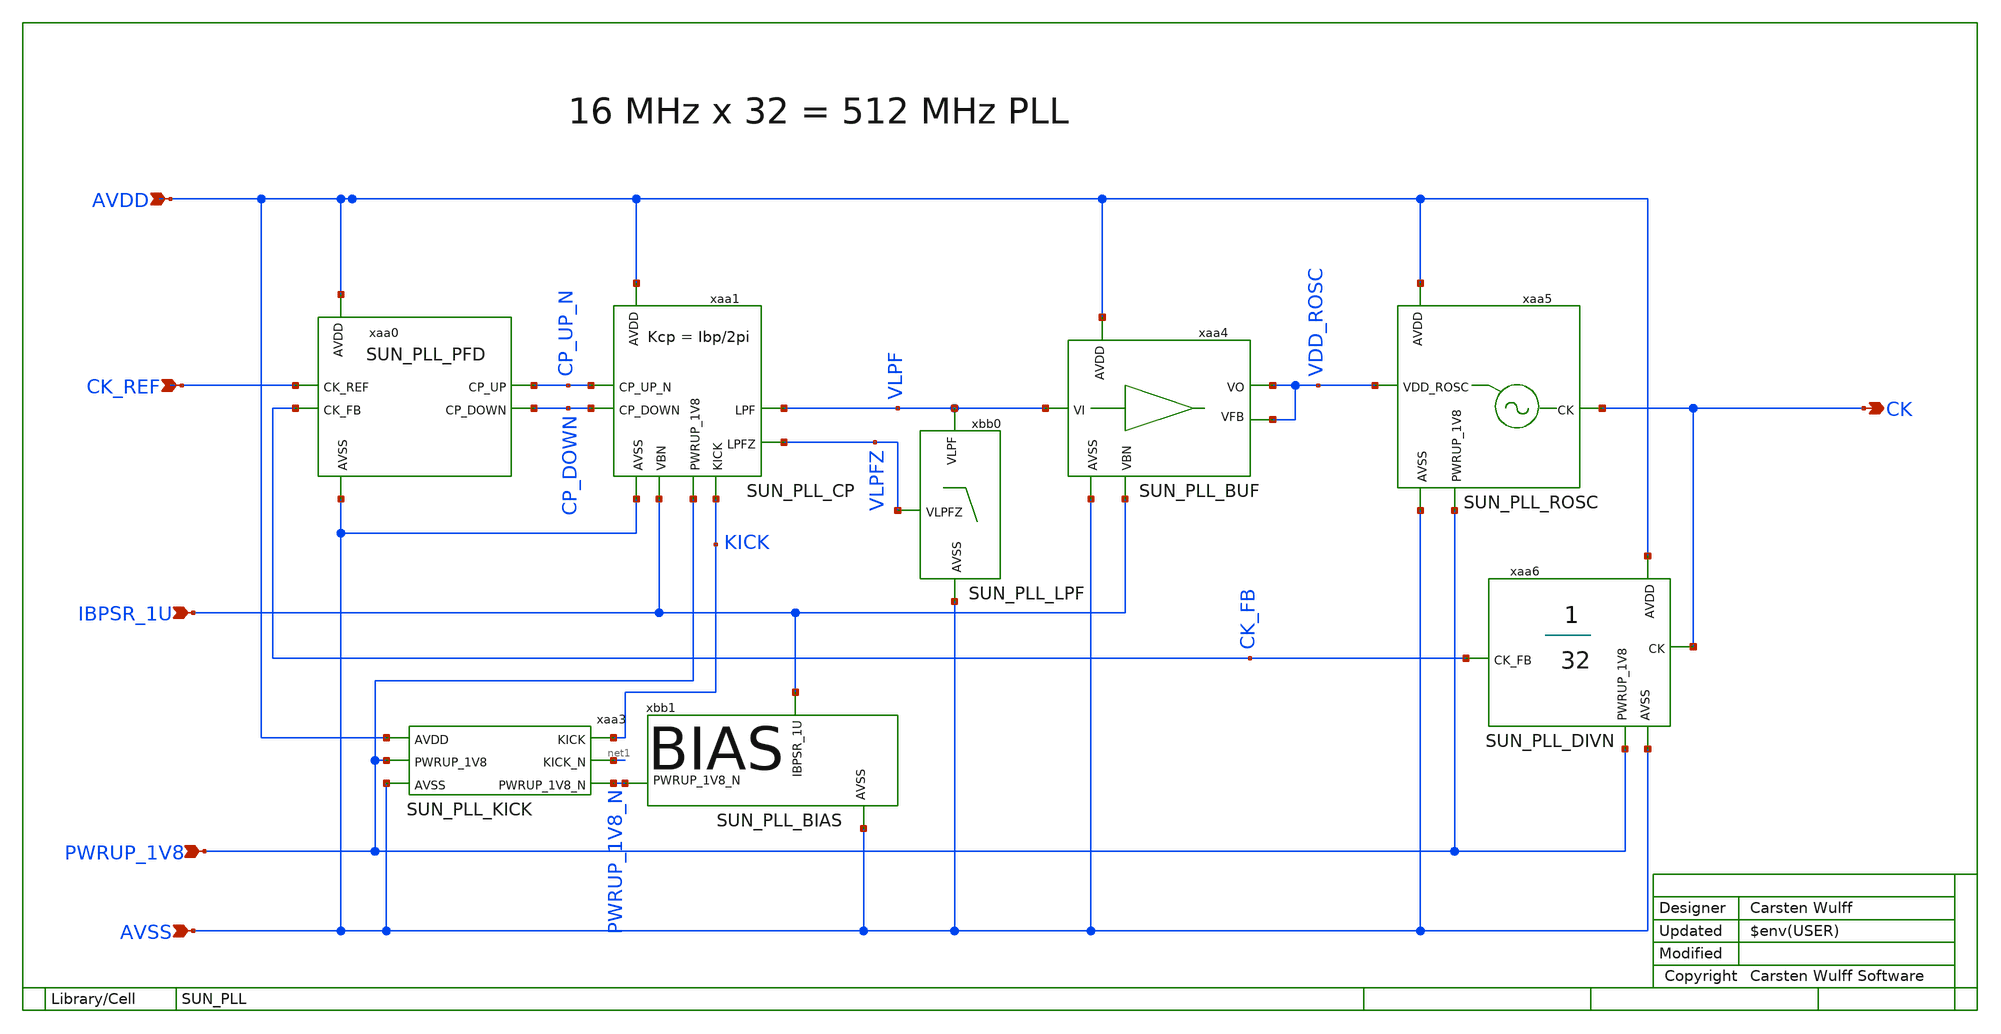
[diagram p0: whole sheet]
** sch_path: ip/sun_pll_sky130nm/design/SUN_PLL_SKY130NM/SUN_PLL.sch
**.subckt SUN_PLL AVDD AVSS PWRUP_1V8 CK_REF CK IBPSR_1U
*.ipin AVDD
*.ipin AVSS
*.ipin PWRUP_1V8
*.ipin CK_REF
*.opin CK
*.ipin IBPSR_1U
xaa5 AVDD CK VDD_ROSC PWRUP_1V8 AVSS SUN_PLL_ROSC xoffset=5 yoffset=0 angle=0
xaa6 AVDD CK_FB CK PWRUP_1V8 AVSS SUN_PLL_DIVN xoffset=-310 yoffset=0 angle=0
xbb1 IBPSR_1U PWRUP_1V8_N AVSS SUN_PLL_BIAS xoffset=5 yoffset=0 angle=0
xaa4 AVDD VDD_ROSC VLPF VDD_ROSC IBPSR_1U AVSS SUN_PLL_BUF xoffset=0 yoffset=0 angle=0
xbb0 VLPFZ AVSS VLPF SUN_PLL_LPF xoffset=0 yoffset=5 angle=0
xaa1 AVDD CP_UP_N VLPF CP_DOWN IBPSR_1U AVSS VLPFZ PWRUP_1V8 KICK SUN_PLL_CP xoffset=0 yoffset=5
+ angle=0
xaa0 AVDD CP_UP_N CK_REF CP_DOWN CK_FB AVSS SUN_PLL_PFD
xaa3 AVDD KICK net1 PWRUP_1V8 AVSS PWRUP_1V8_N SUN_PLL_KICK xoffset=20 yoffset=0 angle=0
**.ends
.end
